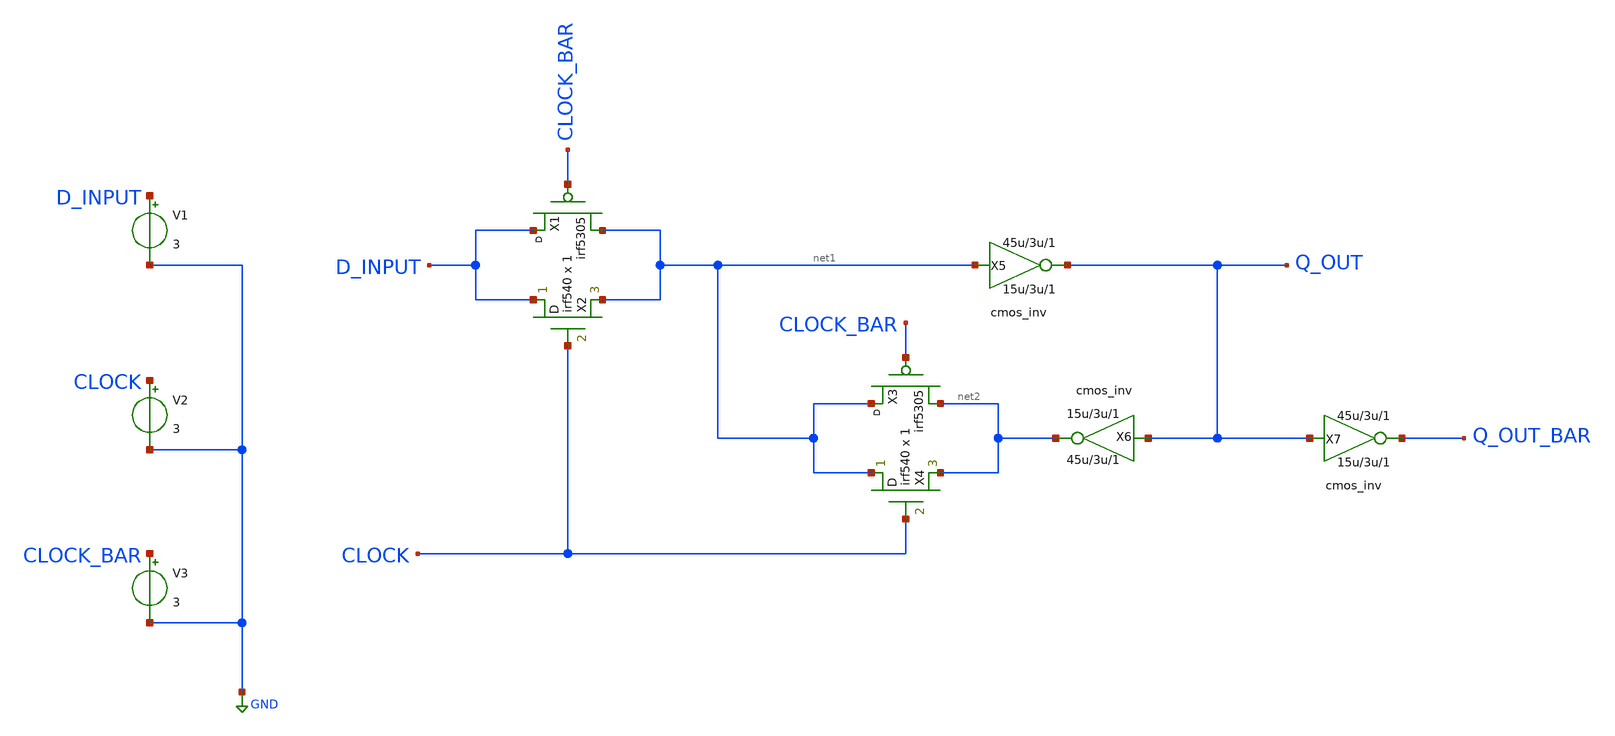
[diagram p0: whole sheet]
** sch_path: Analog_design_files/INV_EXP/hp_inv.sch
* StefanSchippers/xschem/xschem_library/examples/cmos_inv.sch:
* Copyright (C) 1998-2023 Stefan Frederik Schippers
* This program is free software; you can redistribute it and/or modify
* it under the terms of the GNU General Public License as published by
* the Free Software Foundation; either version 2 of the License, or
* (at your option) any later version.
**.subckt hp_inv
X1 D_INPUT CLOCK_BAR net1 irf5305
X2 D_INPUT CLOCK net1 irf540 m=1
X3 net1 CLOCK_BAR net2 irf5305
X4 net1 CLOCK net2 irf540 m=1
X5 Q_OUT net1 cmos_inv WN=15u WP=45u LLN=3u LLP=3u m=1
X6 net2 Q_OUT cmos_inv WN=15u WP=45u LLN=3u LLP=3u m=1
X7 Q_OUT_BAR Q_OUT cmos_inv WN=15u WP=45u LLN=3u LLP=3u m=1
V2 CLOCK GND 3
V3 CLOCK_BAR GND 3
V1 D_INPUT GND 3
**.ends

* expanding   symbol:  cmos_inv.sym # of pins=2
** sym_path: cmos_inv.sym
** sch_path: cmos_inv.sch
.subckt cmos_inv Z A  WN=15u WP=45u LLN=3u LLP=3u
*.opin Z
*.ipin A
M2 net1 A VDD VDD p w=WP l=LLP m=1
M1 D A 0 0 n w=WN l=LLN m=1
R1 net2 D 10 m=1
V1 net1 D 0
.save i(v1)
Vmeas net2 Z 0
.save i(vmeas)
.ends

.GLOBAL GND
.GLOBAL VDD
.end
